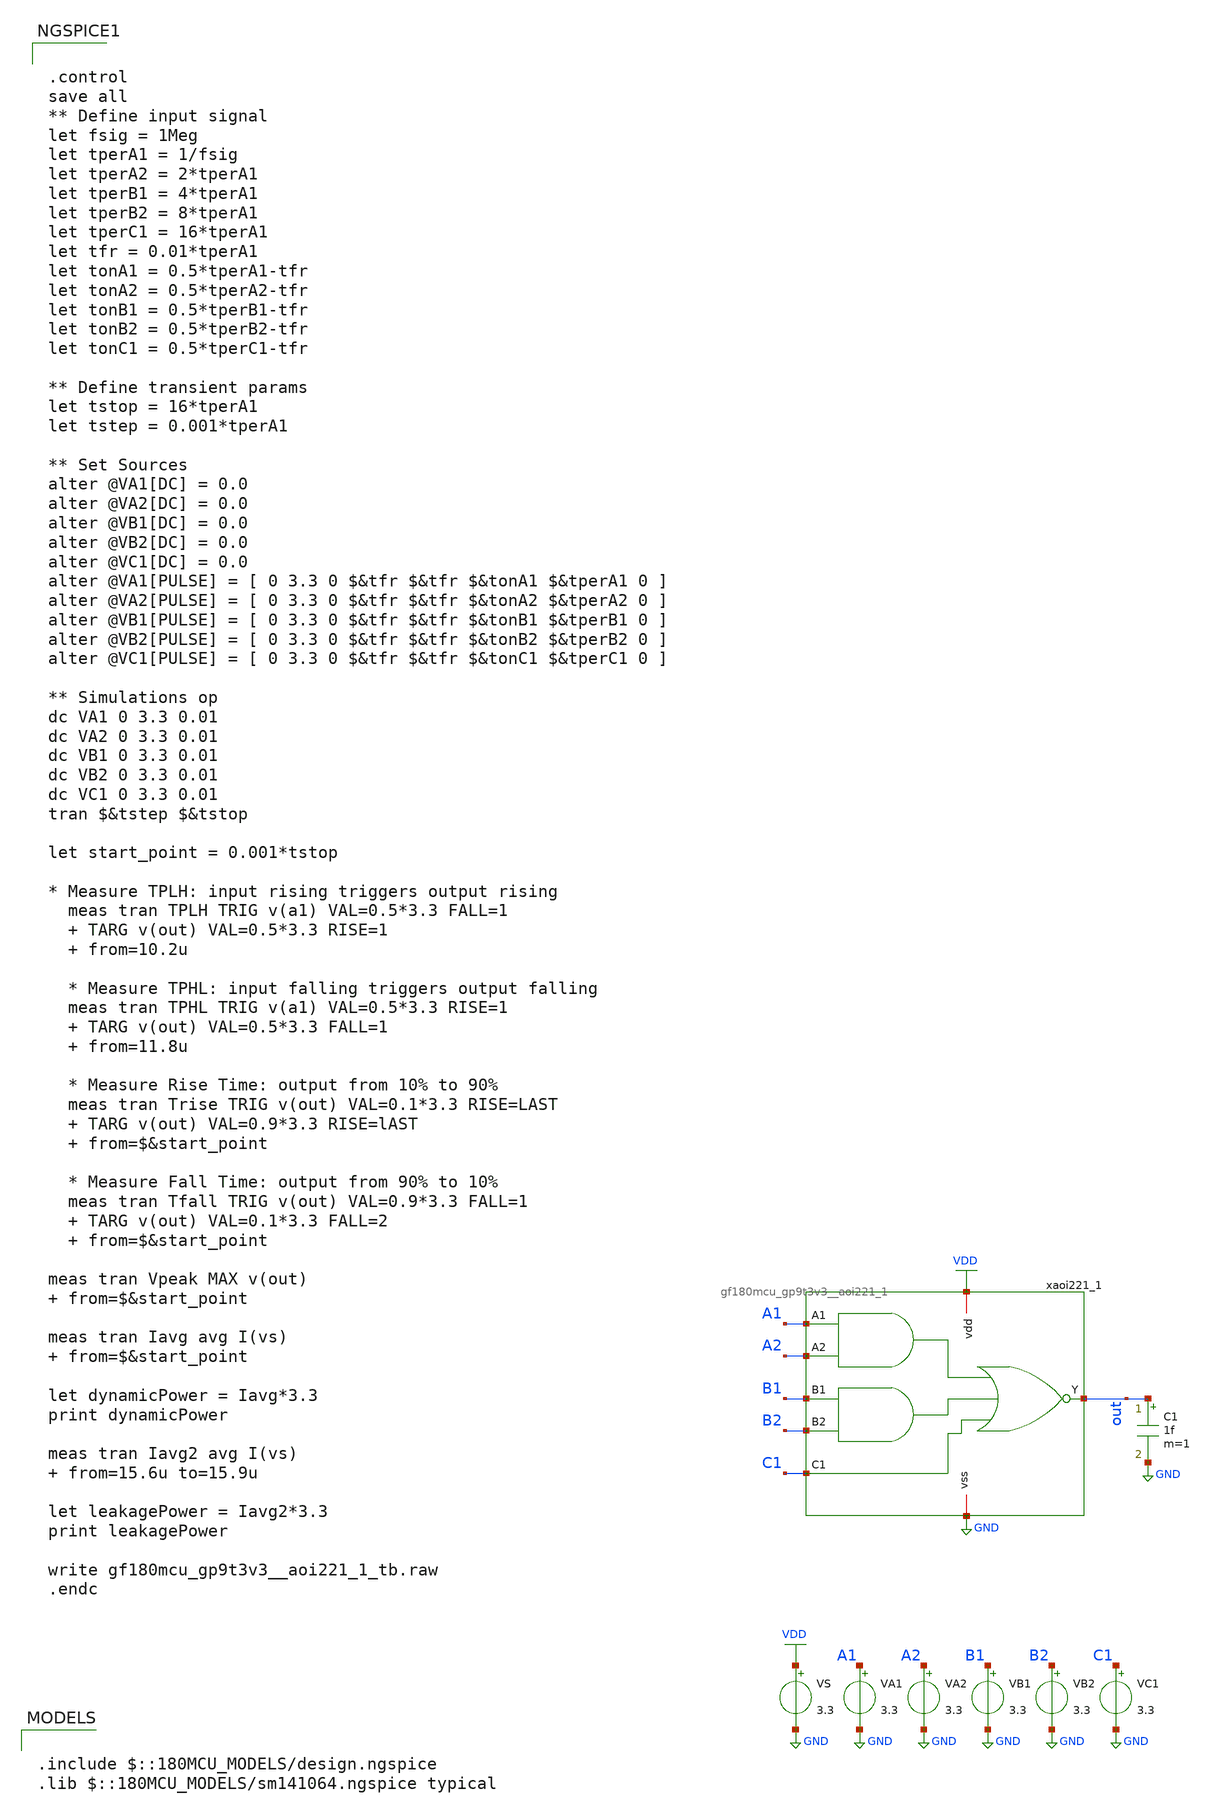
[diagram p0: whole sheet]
** sch_path: designs/aoi221/gf180mcu_gp9t3v3__aoi221_1_tb.sch
**.subckt gf180mcu_gp9t3v3__aoi221_1_tb
VA1 A1 GND 3.3
VA2 A2 GND 3.3
VB1 B1 GND 3.3
VB2 B2 GND 3.3
VC1 C1 GND 3.3
VS VDD GND 3.3
xaoi221_1 VDD out B1 A1 C1 B2 A2 GND gf180mcu_gp9t3v3__aoi221_1
C1 out GND 1f m=1
**** begin user architecture code

.include $::180MCU_MODELS/design.ngspice
.lib $::180MCU_MODELS/sm141064.ngspice typical



.control
save all
** Define input signal
let fsig = 1Meg
let tperA1 = 1/fsig
let tperA2 = 2*tperA1
let tperB1 = 4*tperA1
let tperB2 = 8*tperA1
let tperC1 = 16*tperA1
let tfr = 0.01*tperA1
let tonA1 = 0.5*tperA1-tfr
let tonA2 = 0.5*tperA2-tfr
let tonB1 = 0.5*tperB1-tfr
let tonB2 = 0.5*tperB2-tfr
let tonC1 = 0.5*tperC1-tfr

** Define transient params
let tstop = 16*tperA1
let tstep = 0.001*tperA1

** Set Sources
alter @VA1[DC] = 0.0
alter @VA2[DC] = 0.0
alter @VB1[DC] = 0.0
alter @VB2[DC] = 0.0
alter @VC1[DC] = 0.0
alter @VA1[PULSE] = [ 0 3.3 0 $&tfr $&tfr $&tonA1 $&tperA1 0 ]
alter @VA2[PULSE] = [ 0 3.3 0 $&tfr $&tfr $&tonA2 $&tperA2 0 ]
alter @VB1[PULSE] = [ 0 3.3 0 $&tfr $&tfr $&tonB1 $&tperB1 0 ]
alter @VB2[PULSE] = [ 0 3.3 0 $&tfr $&tfr $&tonB2 $&tperB2 0 ]
alter @VC1[PULSE] = [ 0 3.3 0 $&tfr $&tfr $&tonC1 $&tperC1 0 ]

** Simulations op
dc VA1 0 3.3 0.01
dc VA2 0 3.3 0.01
dc VB1 0 3.3 0.01
dc VB2 0 3.3 0.01
dc VC1 0 3.3 0.01
tran $&tstep $&tstop

let start_point = 0.001*tstop

* Measure TPLH: input rising triggers output rising
  meas tran TPLH TRIG v(a1) VAL=0.5*3.3 FALL=1
  + TARG v(out) VAL=0.5*3.3 RISE=1
  + from=10.2u

  * Measure TPHL: input falling triggers output falling
  meas tran TPHL TRIG v(a1) VAL=0.5*3.3 RISE=1
  + TARG v(out) VAL=0.5*3.3 FALL=1
  + from=11.8u

  * Measure Rise Time: output from 10% to 90%
  meas tran Trise TRIG v(out) VAL=0.1*3.3 RISE=LAST
  + TARG v(out) VAL=0.9*3.3 RISE=lAST
  + from=$&start_point

  * Measure Fall Time: output from 90% to 10%
  meas tran Tfall TRIG v(out) VAL=0.9*3.3 FALL=1
  + TARG v(out) VAL=0.1*3.3 FALL=2
  + from=$&start_point

meas tran Vpeak MAX v(out)  from=$&start_point

meas tran Iavg avg I(vs)  from=$&start_point

let dynamicPower = Iavg*3.3
print dynamicPower

meas tran Iavg2 avg I(vs)  from=15.6u to=15.9u

let leakagePower = Iavg2*3.3
print leakagePower

write gf180mcu_gp9t3v3__aoi221_1_tb.raw
.endc


**** end user architecture code
**.ends

* expanding   symbol:  gf180mcu_gp9t3v3__aoi221_1.sym # of pins=8
** sym_path: designs/aoi221/gf180mcu_gp9t3v3__aoi221_1.sym
** sch_path: designs/aoi221/gf180mcu_gp9t3v3__aoi221_1.sch
.subckt gf180mcu_gp9t3v3__aoi221_1 vdd Y B1 A1 C1 B2 A2 vss
*.iopin vdd
*.iopin vss
*.ipin A1
*.ipin A2
*.ipin B2
*.ipin B1
*.ipin C1
*.opin Y
XM1 Y A1 net1 vss nfet_03v3 L=0.3u W=1u nf=1 ad='int((nf+1)/2) * W/nf * 0.18u' as='int((nf+2)/2) * W/nf * 0.18u'
+ pd='2*int((nf+1)/2) * (W/nf + 0.18u)' ps='2*int((nf+2)/2) * (W/nf + 0.18u)' nrd='0.18u / W' nrs='0.18u / W'
+ sa=0 sb=0 sd=0 m=1
XM2 net1 A2 vss vss nfet_03v3 L=0.3u W=1u nf=1 ad='int((nf+1)/2) * W/nf * 0.18u' as='int((nf+2)/2) * W/nf * 0.18u'
+ pd='2*int((nf+1)/2) * (W/nf + 0.18u)' ps='2*int((nf+2)/2) * (W/nf + 0.18u)' nrd='0.18u / W' nrs='0.18u / W'
+ sa=0 sb=0 sd=0 m=1
XM3 Y B1 net2 vss nfet_03v3 L=0.3u W=1u nf=1 ad='int((nf+1)/2) * W/nf * 0.18u' as='int((nf+2)/2) * W/nf * 0.18u'
+ pd='2*int((nf+1)/2) * (W/nf + 0.18u)' ps='2*int((nf+2)/2) * (W/nf + 0.18u)' nrd='0.18u / W' nrs='0.18u / W'
+ sa=0 sb=0 sd=0 m=1
XM4 net2 B2 vss vss nfet_03v3 L=0.3u W=1u nf=1 ad='int((nf+1)/2) * W/nf * 0.18u' as='int((nf+2)/2) * W/nf * 0.18u'
+ pd='2*int((nf+1)/2) * (W/nf + 0.18u)' ps='2*int((nf+2)/2) * (W/nf + 0.18u)' nrd='0.18u / W' nrs='0.18u / W'
+ sa=0 sb=0 sd=0 m=1
XM5 Y C1 vss vss nfet_03v3 L=0.3u W=0.5u nf=1 ad='int((nf+1)/2) * W/nf * 0.18u' as='int((nf+2)/2) * W/nf * 0.18u'
+ pd='2*int((nf+1)/2) * (W/nf + 0.18u)' ps='2*int((nf+2)/2) * (W/nf + 0.18u)' nrd='0.18u / W' nrs='0.18u / W'
+ sa=0 sb=0 sd=0 m=1
XM6 net4 A1 vdd vdd pfet_03v3 L=0.3u W=2.25u nf=1 ad='int((nf+1)/2) * W/nf * 0.18u' as='int((nf+2)/2) * W/nf * 0.18u'
+ pd='2*int((nf+1)/2) * (W/nf + 0.18u)' ps='2*int((nf+2)/2) * (W/nf + 0.18u)' nrd='0.18u / W' nrs='0.18u / W'
+ sa=0 sb=0 sd=0 m=1
XM7 net4 A2 vdd vdd pfet_03v3 L=0.3u W=2.25u nf=1 ad='int((nf+1)/2) * W/nf * 0.18u' as='int((nf+2)/2) * W/nf * 0.18u'
+ pd='2*int((nf+1)/2) * (W/nf + 0.18u)' ps='2*int((nf+2)/2) * (W/nf + 0.18u)' nrd='0.18u / W' nrs='0.18u / W'
+ sa=0 sb=0 sd=0 m=1
XM8 net3 B1 net4 vdd pfet_03v3 L=0.3u W=2.25u nf=1 ad='int((nf+1)/2) * W/nf * 0.18u' as='int((nf+2)/2) * W/nf * 0.18u'
+ pd='2*int((nf+1)/2) * (W/nf + 0.18u)' ps='2*int((nf+2)/2) * (W/nf + 0.18u)' nrd='0.18u / W' nrs='0.18u / W'
+ sa=0 sb=0 sd=0 m=1
XM9 net3 B2 net4 vdd pfet_03v3 L=0.3u W=2.25u nf=1 ad='int((nf+1)/2) * W/nf * 0.18u' as='int((nf+2)/2) * W/nf * 0.18u'
+ pd='2*int((nf+1)/2) * (W/nf + 0.18u)' ps='2*int((nf+2)/2) * (W/nf + 0.18u)' nrd='0.18u / W' nrs='0.18u / W'
+ sa=0 sb=0 sd=0 m=1
XM10 Y C1 net3 vdd pfet_03v3 L=0.3u W=2.25u nf=1 ad='int((nf+1)/2) * W/nf * 0.18u' as='int((nf+2)/2) * W/nf * 0.18u'
+ pd='2*int((nf+1)/2) * (W/nf + 0.18u)' ps='2*int((nf+2)/2) * (W/nf + 0.18u)' nrd='0.18u / W' nrs='0.18u / W'
+ sa=0 sb=0 sd=0 m=1
.ends

.GLOBAL VDD
.GLOBAL GND
.end
